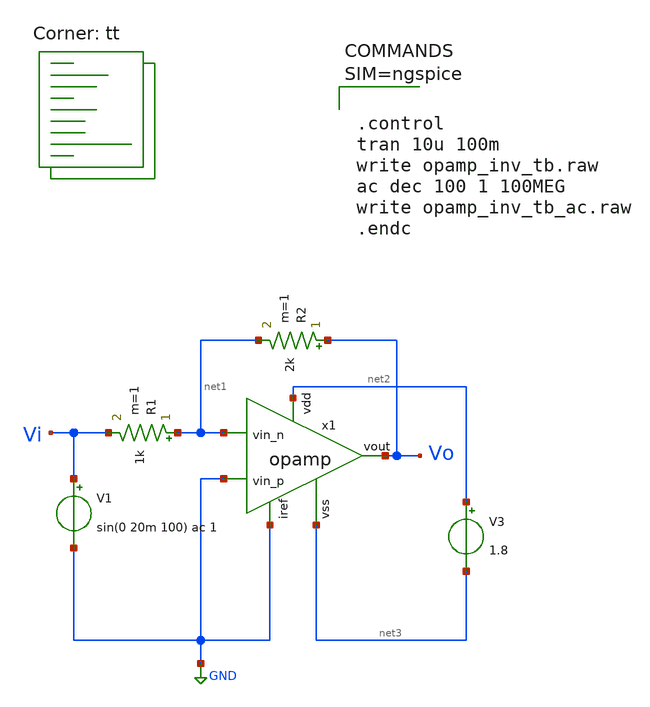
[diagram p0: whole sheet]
** sch_path: xschem/opamp_inv_tb.sch
**.subckt opamp_inv_tb
x1 net2 GND net1 GND Vo net3 opamp
R1 net1 Vi 1k m=1
R2 Vo net1 2k m=1
V1 Vi GND sin(0 20m 100) ac 1
V3 net2 net3 1.8
**** begin user architecture code



.control
tran 10u 100m
write opamp_inv_tb.raw
ac dec 100 1 100MEG
write opamp_inv_tb_ac.raw
.endc



.lib $::SKYWATER_MODELS/sky130.lib.spice tt
**** end user architecture code
**.ends
.GLOBAL GND
.end
